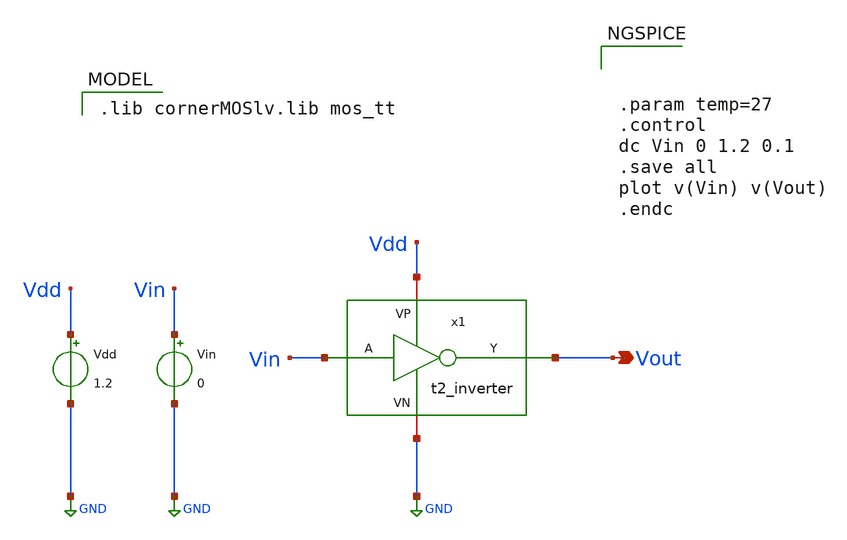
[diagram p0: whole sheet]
** sch_path: Team Designs/Team 2 Design/design_data/xschem/t2_inverter_tb_dc.sch
**.subckt t2_inverter_tb_dc Vout
*.opin Vout
Vin Vin GND 0
Vdd Vdd GND 1.2
x1 Vdd Vin Vout GND t2_inverter
**** begin user architecture code
 .lib cornerMOSlv.lib mos_tt




.param temp=27
.control
dc Vin 0 1.2 0.1
.save all
plot v(Vin) v(Vout)
.endc


**** end user architecture code
**.ends

* expanding   symbol:  /foss/designs/IHP/Inverter/t2_inverter.sym # of pins=4
** sym_path: Team 2 Design/design_data/xschem/t2_inverter.sym
** sch_path: Team 2 Design/design_data/xschem/t2_inverter.sch
.subckt t2_inverter VP A Y VN
*.iopin VP
*.iopin VN
*.ipin A
*.opin Y
XM2 Y A VP VP sg13_lv_pmos w=0.3u l=0.13u ng=1 m=1 mm_ok=1
XM1 Y A VN VN sg13_lv_nmos w=0.15u l=0.13u ng=1 m=1 mm_ok=1
.ends

.GLOBAL GND
.end
